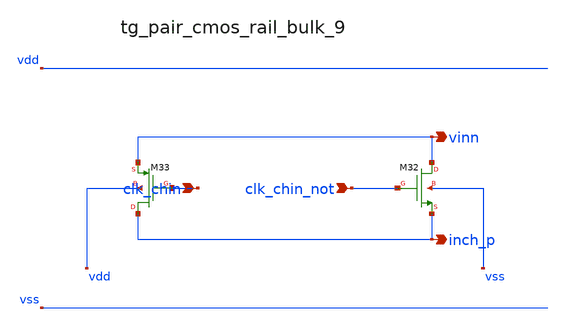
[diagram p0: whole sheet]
** sch_path: analog-db/raw/ia_002_fan_chopper_simple/hier/blocks/tg_pair_cmos_rail_bulk_9.sch
**.subckt tg_pair_cmos_rail_bulk_9 clk_chin clk_chin_not vinn inch_p
*.ipin clk_chin
*.ipin clk_chin_not
*.opin vinn
*.opin inch_p
XM32 vinn clk_chin_not inch_p vss sg13_lv_nmos w=x_dut_xm32_w l=x_dut_xm32_l ng=1 m=x_dut_xm32_m
XM33 inch_p clk_chin vinn vdd sg13_lv_pmos w=x_dut_xm33_w l=x_dut_xm33_l ng=1 m=x_dut_xm33_m
**.ends
.end
